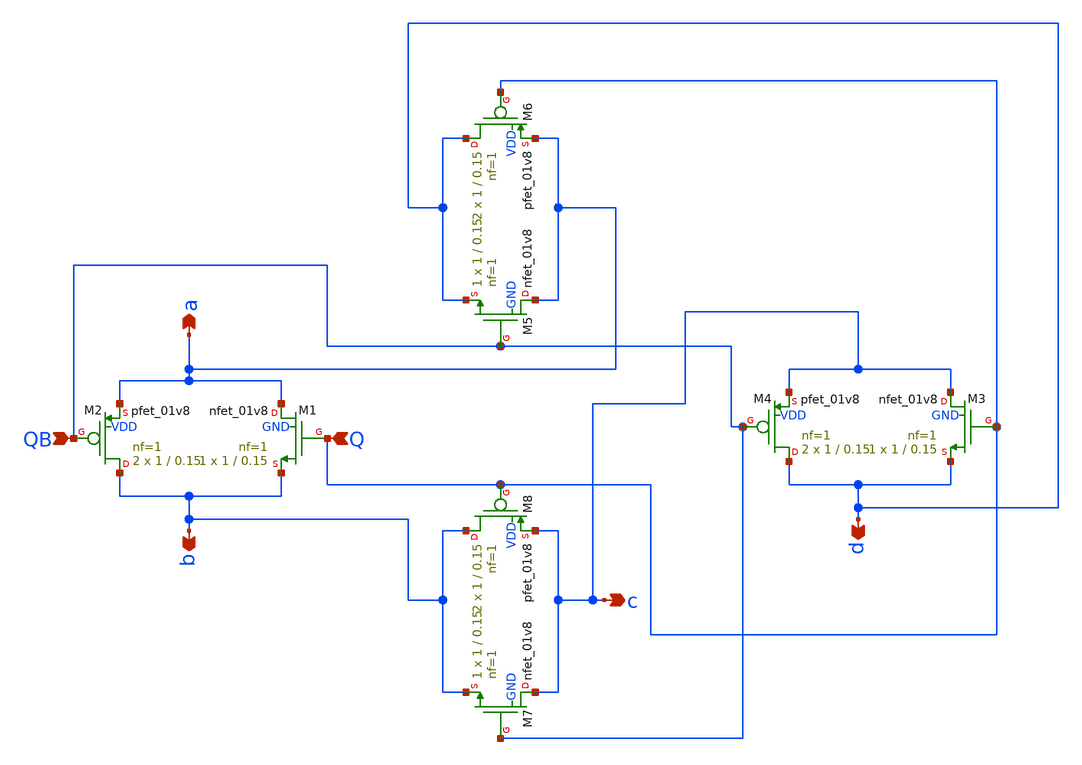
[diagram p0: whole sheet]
** sch_path: chopper.sch
**.subckt chopper QB Q a d b c
*.ipin QB
*.ipin Q
*.opin a
*.opin d
*.opin b
*.opin c
XM1 a Q b GND sky130_fd_pr__nfet_01v8 L=0.15 W=1 nf=1 ad='int((nf+1)/2) * W/nf * 0.29' as='int((nf+2)/2) * W/nf * 0.29'
+ pd='2*int((nf+1)/2) * (W/nf + 0.29)' ps='2*int((nf+2)/2) * (W/nf + 0.29)' nrd='0.29 / W' nrs='0.29 / W'
+ sa=0 sb=0 sd=0 mult=1 m=1
XM2 b QB a VDD sky130_fd_pr__pfet_01v8 L=0.15 W=1 nf=1 ad='int((nf+1)/2) * W/nf * 0.29' as='int((nf+2)/2) * W/nf * 0.29'
+ pd='2*int((nf+1)/2) * (W/nf + 0.29)' ps='2*int((nf+2)/2) * (W/nf + 0.29)' nrd='0.29 / W' nrs='0.29 / W'
+ sa=0 sb=0 sd=0 mult=2 m=2
XM3 c Q d GND sky130_fd_pr__nfet_01v8 L=0.15 W=1 nf=1 ad='int((nf+1)/2) * W/nf * 0.29' as='int((nf+2)/2) * W/nf * 0.29'
+ pd='2*int((nf+1)/2) * (W/nf + 0.29)' ps='2*int((nf+2)/2) * (W/nf + 0.29)' nrd='0.29 / W' nrs='0.29 / W'
+ sa=0 sb=0 sd=0 mult=1 m=1
XM4 d QB c VDD sky130_fd_pr__pfet_01v8 L=0.15 W=1 nf=1 ad='int((nf+1)/2) * W/nf * 0.29' as='int((nf+2)/2) * W/nf * 0.29'
+ pd='2*int((nf+1)/2) * (W/nf + 0.29)' ps='2*int((nf+2)/2) * (W/nf + 0.29)' nrd='0.29 / W' nrs='0.29 / W'
+ sa=0 sb=0 sd=0 mult=2 m=2
XM5 a QB d GND sky130_fd_pr__nfet_01v8 L=0.15 W=1 nf=1 ad='int((nf+1)/2) * W/nf * 0.29' as='int((nf+2)/2) * W/nf * 0.29'
+ pd='2*int((nf+1)/2) * (W/nf + 0.29)' ps='2*int((nf+2)/2) * (W/nf + 0.29)' nrd='0.29 / W' nrs='0.29 / W'
+ sa=0 sb=0 sd=0 mult=1 m=1
XM6 d Q a VDD sky130_fd_pr__pfet_01v8 L=0.15 W=1 nf=1 ad='int((nf+1)/2) * W/nf * 0.29' as='int((nf+2)/2) * W/nf * 0.29'
+ pd='2*int((nf+1)/2) * (W/nf + 0.29)' ps='2*int((nf+2)/2) * (W/nf + 0.29)' nrd='0.29 / W' nrs='0.29 / W'
+ sa=0 sb=0 sd=0 mult=2 m=2
XM7 c QB b GND sky130_fd_pr__nfet_01v8 L=0.15 W=1 nf=1 ad='int((nf+1)/2) * W/nf * 0.29' as='int((nf+2)/2) * W/nf * 0.29'
+ pd='2*int((nf+1)/2) * (W/nf + 0.29)' ps='2*int((nf+2)/2) * (W/nf + 0.29)' nrd='0.29 / W' nrs='0.29 / W'
+ sa=0 sb=0 sd=0 mult=1 m=1
XM8 b Q c VDD sky130_fd_pr__pfet_01v8 L=0.15 W=1 nf=1 ad='int((nf+1)/2) * W/nf * 0.29' as='int((nf+2)/2) * W/nf * 0.29'
+ pd='2*int((nf+1)/2) * (W/nf + 0.29)' ps='2*int((nf+2)/2) * (W/nf + 0.29)' nrd='0.29 / W' nrs='0.29 / W'
+ sa=0 sb=0 sd=0 mult=2 m=2
**.ends
.end
